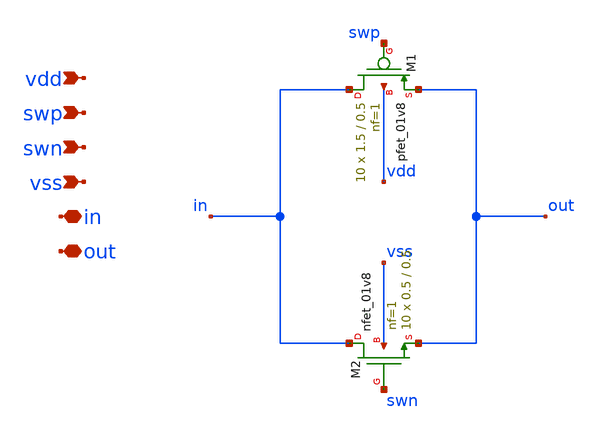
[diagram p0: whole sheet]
** sch_path: xschem/tg_sw_6.sch
**.subckt tg_sw_6 vdd swp swn vss in out
*.ipin vdd
*.ipin swp
*.ipin swn
*.ipin vss
*.iopin in
*.iopin out
XM1 in swp out vdd sky130_fd_pr__pfet_01v8 L=0.5 W=1.5 nf=1 ad='int((nf+1)/2) * W/nf * 0.29' as='int((nf+2)/2) * W/nf * 0.29'
+ pd='2*int((nf+1)/2) * (W/nf + 0.29)' ps='2*int((nf+2)/2) * (W/nf + 0.29)' nrd='0.29 / W' nrs='0.29 / W'
+ sa=0 sb=0 sd=0 mult=10 m=10
XM2 in swn out vss sky130_fd_pr__nfet_01v8 L=0.5 W=0.5 nf=1 ad='int((nf+1)/2) * W/nf * 0.29' as='int((nf+2)/2) * W/nf * 0.29'
+ pd='2*int((nf+1)/2) * (W/nf + 0.29)' ps='2*int((nf+2)/2) * (W/nf + 0.29)' nrd='0.29 / W' nrs='0.29 / W'
+ sa=0 sb=0 sd=0 mult=10 m=10
**.ends
.end
